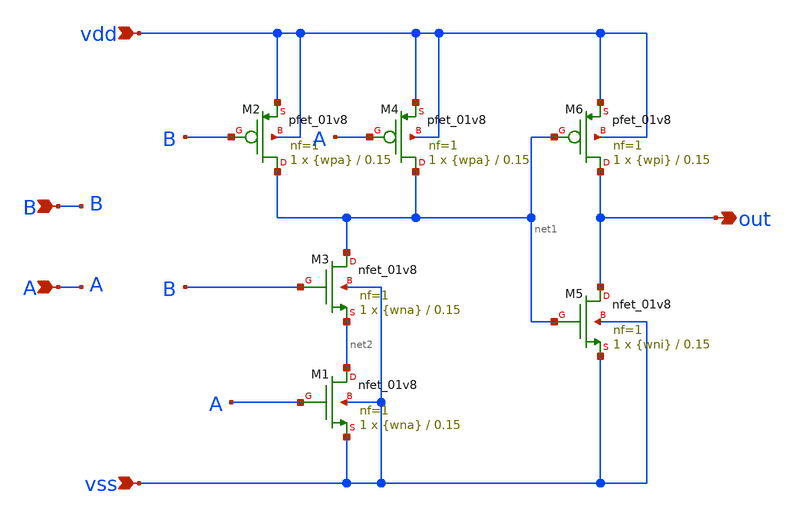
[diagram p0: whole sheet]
** sch_path: src/and/and.sch
**.subckt and vdd vss out B A
*.ipin vdd
*.ipin vss
*.opin out
*.ipin B
*.ipin A
XM1 net2 A vss vss sky130_fd_pr__nfet_01v8 L=0.15 W={wna} nf=1 ad='int((nf+1)/2) * W/nf * 0.29' as='int((nf+2)/2) * W/nf * 0.29'
+ pd='2*int((nf+1)/2) * (W/nf + 0.29)' ps='2*int((nf+2)/2) * (W/nf + 0.29)' nrd='0.29 / W' nrs='0.29 / W'
+ sa=0 sb=0 sd=0 mult=1 m=1
XM2 net1 B vdd vdd sky130_fd_pr__pfet_01v8 L=0.15 W={wpa} nf=1 ad='int((nf+1)/2) * W/nf * 0.29' as='int((nf+2)/2) * W/nf * 0.29'
+ pd='2*int((nf+1)/2) * (W/nf + 0.29)' ps='2*int((nf+2)/2) * (W/nf + 0.29)' nrd='0.29 / W' nrs='0.29 / W'
+ sa=0 sb=0 sd=0 mult=1 m=1
XM3 net1 B net2 vss sky130_fd_pr__nfet_01v8 L=0.15 W={wna} nf=1 ad='int((nf+1)/2) * W/nf * 0.29' as='int((nf+2)/2) * W/nf * 0.29'
+ pd='2*int((nf+1)/2) * (W/nf + 0.29)' ps='2*int((nf+2)/2) * (W/nf + 0.29)' nrd='0.29 / W' nrs='0.29 / W'
+ sa=0 sb=0 sd=0 mult=1 m=1
XM4 net1 A vdd vdd sky130_fd_pr__pfet_01v8 L=0.15 W={wpa} nf=1 ad='int((nf+1)/2) * W/nf * 0.29' as='int((nf+2)/2) * W/nf * 0.29'
+ pd='2*int((nf+1)/2) * (W/nf + 0.29)' ps='2*int((nf+2)/2) * (W/nf + 0.29)' nrd='0.29 / W' nrs='0.29 / W'
+ sa=0 sb=0 sd=0 mult=1 m=1
XM5 out net1 vss vss sky130_fd_pr__nfet_01v8 L=0.15 W={wni} nf=1 ad='int((nf+1)/2) * W/nf * 0.29' as='int((nf+2)/2) * W/nf * 0.29'
+ pd='2*int((nf+1)/2) * (W/nf + 0.29)' ps='2*int((nf+2)/2) * (W/nf + 0.29)' nrd='0.29 / W' nrs='0.29 / W'
+ sa=0 sb=0 sd=0 mult=1 m=1
XM6 out net1 vdd vdd sky130_fd_pr__pfet_01v8 L=0.15 W={wpi} nf=1 ad='int((nf+1)/2) * W/nf * 0.29' as='int((nf+2)/2) * W/nf * 0.29'
+ pd='2*int((nf+1)/2) * (W/nf + 0.29)' ps='2*int((nf+2)/2) * (W/nf + 0.29)' nrd='0.29 / W' nrs='0.29 / W'
+ sa=0 sb=0 sd=0 mult=1 m=1
**.ends
.end
